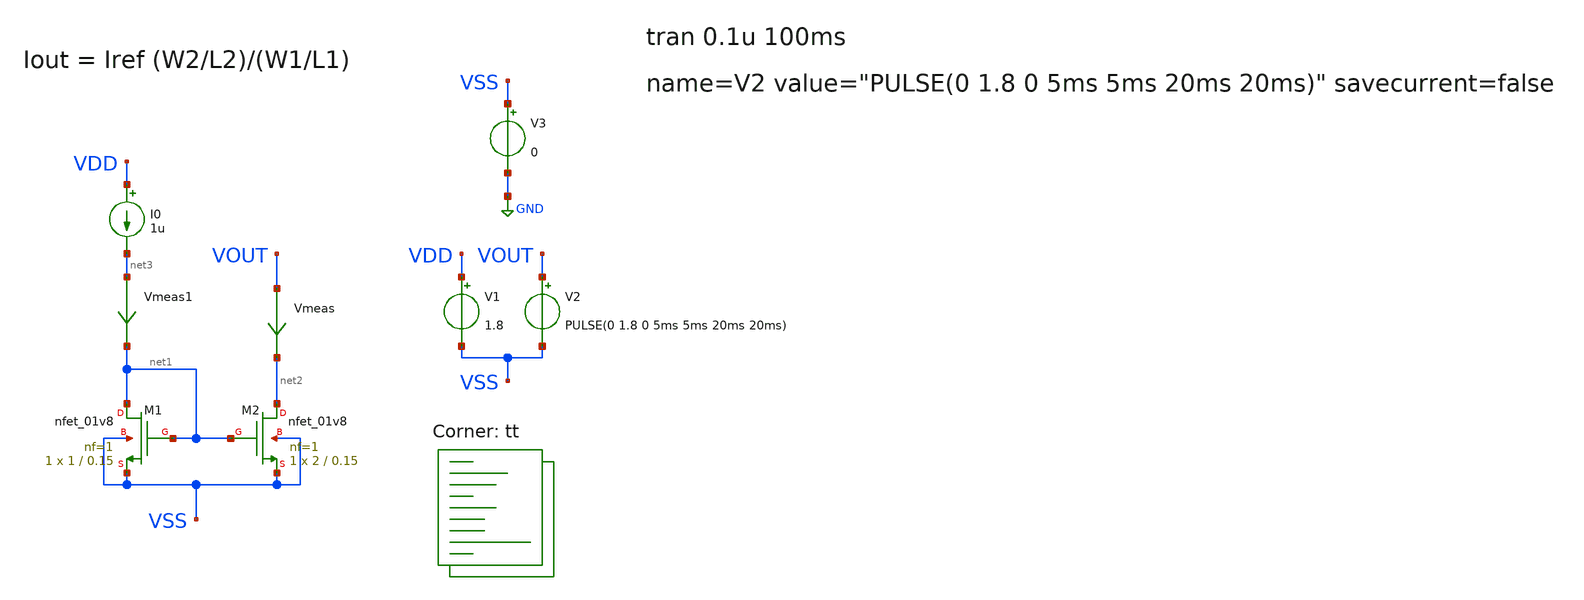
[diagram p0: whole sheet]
** sch_path: week02_current_diffpair/tugas4_basic_current_mirror/nmos-current-mirror.sch
**.subckt nmos-current-mirror
XM1 net1 net1 VSS VSS sky130_fd_pr__nfet_01v8 L=0.15 W=1 nf=1 ad='int((nf+1)/2) * W/nf * 0.29' as='int((nf+2)/2) * W/nf * 0.29'
+ pd='2*int((nf+1)/2) * (W/nf + 0.29)' ps='2*int((nf+2)/2) * (W/nf + 0.29)' nrd='0.29 / W' nrs='0.29 / W'
+ sa=0 sb=0 sd=0 mult=1 m=1
XM2 net2 net1 VSS VSS sky130_fd_pr__nfet_01v8 L=0.15 W=2 nf=1 ad='int((nf+1)/2) * W/nf * 0.29' as='int((nf+2)/2) * W/nf * 0.29'
+ pd='2*int((nf+1)/2) * (W/nf + 0.29)' ps='2*int((nf+2)/2) * (W/nf + 0.29)' nrd='0.29 / W' nrs='0.29 / W'
+ sa=0 sb=0 sd=0 mult=1 m=1
I0 VDD net3 1u
V1 VDD VSS 1.8
V2 VOUT VSS PULSE(0 1.8 0 5ms 5ms 20ms 20ms)
V3 VSS GND 0
Vmeas VOUT net2 0
.save i(vmeas)
Vmeas1 net3 net1 0
.save i(vmeas1)
**** begin user architecture code
.lib $::SKYWATER_MODELS/sky130.lib.spice tt



	.param Wm2=1u

.control
	dc V2 0 0.9 0.01

	plot I(Vmeas)


saveall
.endc


**** end user architecture code
**.ends
.GLOBAL GND
.end
